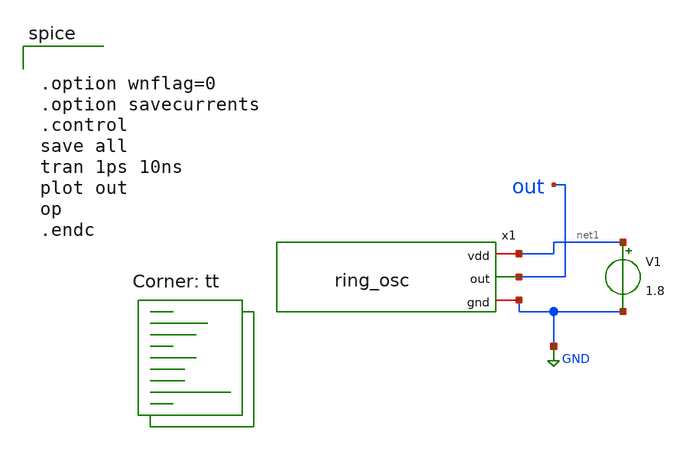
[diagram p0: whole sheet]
** sch_path: ring_osc_tb.sch
**.subckt ring_osc_tb
x1 net1 out GND ring_osc
V1 net1 GND 1.8
**** begin user architecture code


.option wnflag=0
.option savecurrents
.control
save all
tran 1ps 10ns
plot out
op
.endc



** opencircuitdesign pdks install
.lib $::SKYWATER_MODELS/sky130.lib.spice tt

**** end user architecture code
**.ends

* expanding   symbol:  /home/mona121130125/percobaan_layout/ring_osc.sym # of pins=3
** sym_path: ring_osc.sym
** sch_path: ring_osc.sch
.subckt ring_osc vdd out gnd
*.iopin vdd
*.iopin gnd
*.opin out
x1 vdd out net1 gnd inverter
x2 vdd net1 net2 gnd inverter
x3 vdd net2 out gnd inverter
.ends


* expanding   symbol:  /home/mona121130125/percobaan_layout/inverter.sym # of pins=4
** sym_path: inverter.sym
** sch_path: inverter.sch
.subckt inverter vdd in out gnd
*.ipin in
*.opin out
*.iopin vdd
*.iopin gnd
XM1 out in vdd vdd sky130_fd_pr__pfet_01v8 L=0.15 W=1 nf=1 ad='int((nf+1)/2) * W/nf * 0.29' as='int((nf+2)/2) * W/nf * 0.29'
+ pd='2*int((nf+1)/2) * (W/nf + 0.29)' ps='2*int((nf+2)/2) * (W/nf + 0.29)' nrd='0.29 / W' nrs='0.29 / W'
+ sa=0 sb=0 sd=0 mult=1 m=1
XM2 out in gnd gnd sky130_fd_pr__nfet_01v8 L=0.15 W=1 nf=1 ad='int((nf+1)/2) * W/nf * 0.29' as='int((nf+2)/2) * W/nf * 0.29'
+ pd='2*int((nf+1)/2) * (W/nf + 0.29)' ps='2*int((nf+2)/2) * (W/nf + 0.29)' nrd='0.29 / W' nrs='0.29 / W'
+ sa=0 sb=0 sd=0 mult=1 m=1
.ends

.GLOBAL GND
.end
